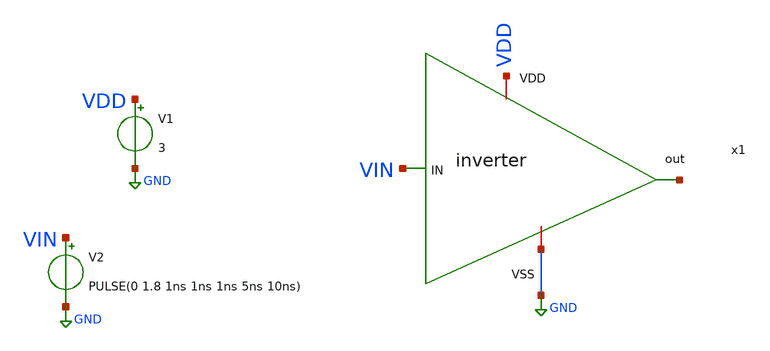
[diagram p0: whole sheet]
** sch_path: tb_inverter.sch
**.subckt tb_inverter
x1 VDD VIN net1 GND inverter
V1 VDD GND 3
V2 VIN GND PULSE(0 1.8 1ns 1ns 1ns 5ns 10ns)
**.ends

* expanding   symbol:  /home/ttuser/Documents/ADCAnalogDesign/inverter.sym # of pins=4
** sym_path: inverter.sym
** sch_path: inverter.sch
.subckt inverter VDD IN out VSS
*.ipin IN
*.opin out
*.iopin VDD
*.iopin VSS
XM3 out IN VDD VDD sky130_fd_pr__pfet_01v8 L=0.15 W=1 nf=1 ad='int((nf+1)/2) * W/nf * 0.29' as='int((nf+2)/2) * W/nf * 0.29'
+ pd='2*int((nf+1)/2) * (W/nf + 0.29)' ps='2*int((nf+2)/2) * (W/nf + 0.29)' nrd='0.29 / W' nrs='0.29 / W'
+ sa=0 sb=0 sd=0 mult=1 m=1
XM2 out IN VSS VSS sky130_fd_pr__nfet_01v8 L=0.15 W=1 nf=1 ad='int((nf+1)/2) * W/nf * 0.29' as='int((nf+2)/2) * W/nf * 0.29'
+ pd='2*int((nf+1)/2) * (W/nf + 0.29)' ps='2*int((nf+2)/2) * (W/nf + 0.29)' nrd='0.29 / W' nrs='0.29 / W'
+ sa=0 sb=0 sd=0 mult=1 m=1
.ends

.GLOBAL GND
.end
